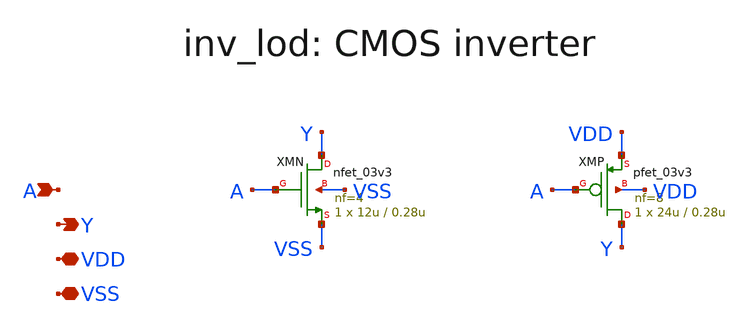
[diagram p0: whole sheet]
** sch_path: v1_claude/archive/legacy_cells/xschem/inv_lod.sch
**.subckt inv_lod A Y VDD VSS
*.ipin A
*.opin Y
*.iopin VDD
*.iopin VSS
XMN Y A VSS VSS nfet_03v3 L=0.28u W=12u nf=4 ad='int((nf+1)/2) * W/nf * 0.18u' as='int((nf+2)/2) * W/nf * 0.18u'
+ pd='2*int((nf+1)/2) * (W/nf + 0.18u)' ps='2*int((nf+2)/2) * (W/nf + 0.18u)' nrd='0.18u / W' nrs='0.18u / W'
+ sa=0 sb=0 sd=0 m=1
XMP Y A VDD VDD pfet_03v3 L=0.28u W=24u nf=8 ad='int((nf+1)/2) * W/nf * 0.18u' as='int((nf+2)/2) * W/nf * 0.18u'
+ pd='2*int((nf+1)/2) * (W/nf + 0.18u)' ps='2*int((nf+2)/2) * (W/nf + 0.18u)' nrd='0.18u / W' nrs='0.18u / W'
+ sa=0 sb=0 sd=0 m=1
**.ends
.end
